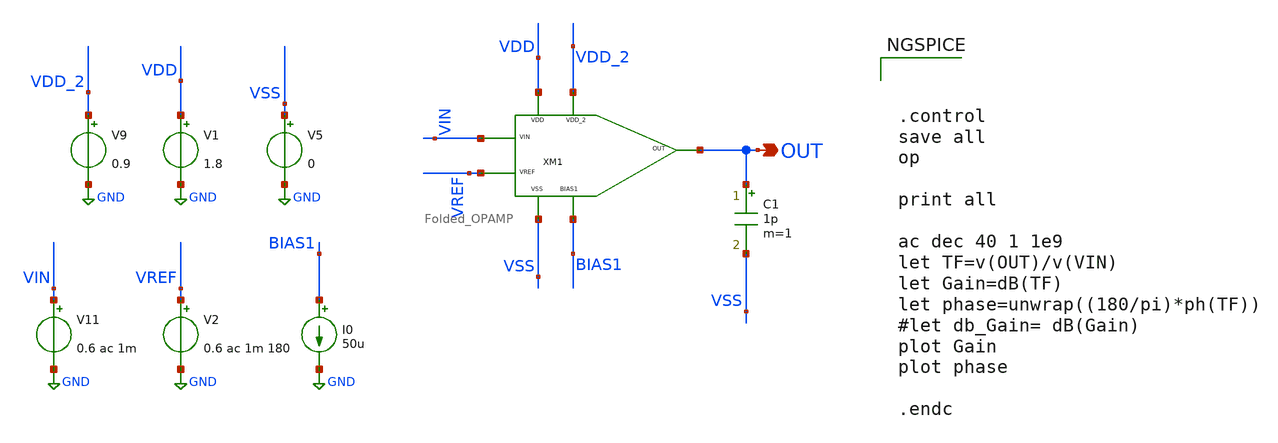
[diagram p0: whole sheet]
** sch_path: xschem/DC_DC_Converter_xschem/OTHERS/DC_DC_Converter_JV8/Folded_OPAMP/tb_Folded_OPAMP.sch
**.subckt tb_Folded_OPAMP OUT
*.opin OUT
I0 BIAS1 GND 50u
V9 VDD_2 GND 0.9
V1 VDD GND 1.8
V5 VSS GND 0
V11 VIN GND 0.6 ac 1m
V2 VREF GND 0.6 ac 1m 180
XM1 VDD VSS VDD_2 BIAS1 OUT VIN VREF Folded_OPAMP
C1 OUT VSS 1p m=1
**** begin user architecture code

** opencircuitdesign pdks install
.lib $::SKYWATER_MODELS/sky130.lib.spice tt





.control
save all
op

print all

ac dec 40 1 1e9
let TF=v(OUT)/v(VIN)
let Gain=dB(TF)
let phase=unwrap((180/pi)*ph(TF))
#let db_Gain= dB(Gain)
plot Gain
plot phase

.endc


**** end user architecture code
**.ends
.GLOBAL GND
.end
